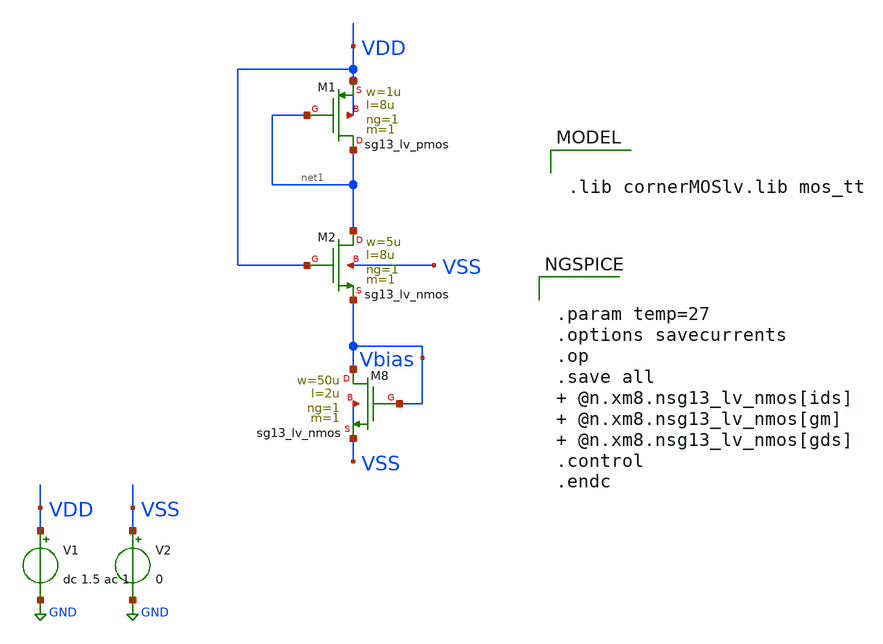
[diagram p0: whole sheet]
** sch_path: designs/1iee34/tailcurrent.sch
**.subckt tailcurrent
V1 VDD GND dc 1.5 ac 1
V2 VSS GND 0
XM8 Vbias Vbias VSS VSS sg13_lv_nmos w=50u l=2u ng=1 m=1 mm_ok=1
XM1 net1 net1 VDD VDD sg13_lv_pmos w=1u l=8u ng=1 m=1 mm_ok=1
XM2 net1 VDD Vbias VSS sg13_lv_nmos w=5u l=8u ng=1 m=1 mm_ok=1
**** begin user architecture code


.param temp=27
.options savecurrents
.op
.save all  @n.xm8.nsg13_lv_nmos[ids]  @n.xm8.nsg13_lv_nmos[gm]  @n.xm8.nsg13_lv_nmos[gds]
.control
.endc




.lib cornerMOSlv.lib mos_tt


**** end user architecture code
**.ends
.GLOBAL GND
.end
